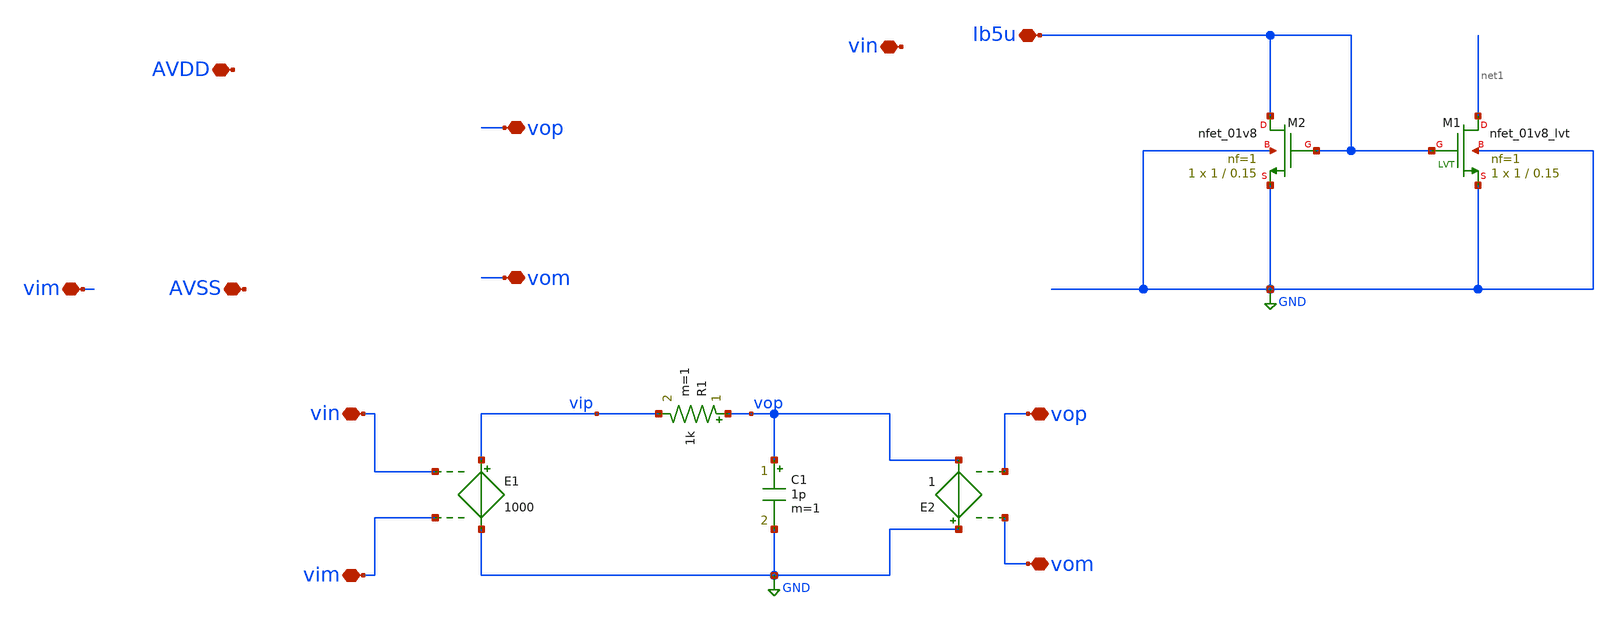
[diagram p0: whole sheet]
** sch_path: xschem/opampnew.sch
**.subckt opampnew vim vin vom vop AVDD AVSS vim vin vom vop Ib5u
*.iopin vim
*.iopin vin
*.iopin vom
*.iopin vop
*.iopin AVDD
*.iopin AVSS
*.iopin vim
*.iopin vin
*.iopin vom
*.iopin vop
*.iopin Ib5u
E1 vip GND vin vim 1000
E2 GND vop vom vop 1
R1 vop vip 1k m=1
C1 vop GND 1p m=1
XM1 net1 Ib5u GND GND sky130_fd_pr__nfet_01v8_lvt L=0.15 W=1 nf=1 ad='int((1 + 1)/2) * 1 / 1 * 0.29'
+ as='int((1 + 2)/2) * 1 / 1 * 0.29' pd='2*int((1 + 1)/2) * (1 / 1 + 0.29)' ps='2*int((1 + 2)/2) * (1 / 1 + 0.29)'
+ nrd='0.29 / 1 ' nrs='0.29 / 1 ' sa=0 sb=0 sd=0 mult=1 m=1
XM2 Ib5u Ib5u GND GND sky130_fd_pr__nfet_01v8 L=0.15 W=1 nf=1 ad='int((1 + 1)/2) * 1 / 1 * 0.29' as='int((1 + 2)/2) * 1 / 1 * 0.29'
+ pd='2*int((1 + 1)/2) * (1 / 1 + 0.29)' ps='2*int((1 + 2)/2) * (1 / 1 + 0.29)' nrd='0.29 / 1 ' nrs='0.29 / 1 '
+ sa=0 sb=0 sd=0 mult=1 m=1
**.ends
.GLOBAL GND
.end
